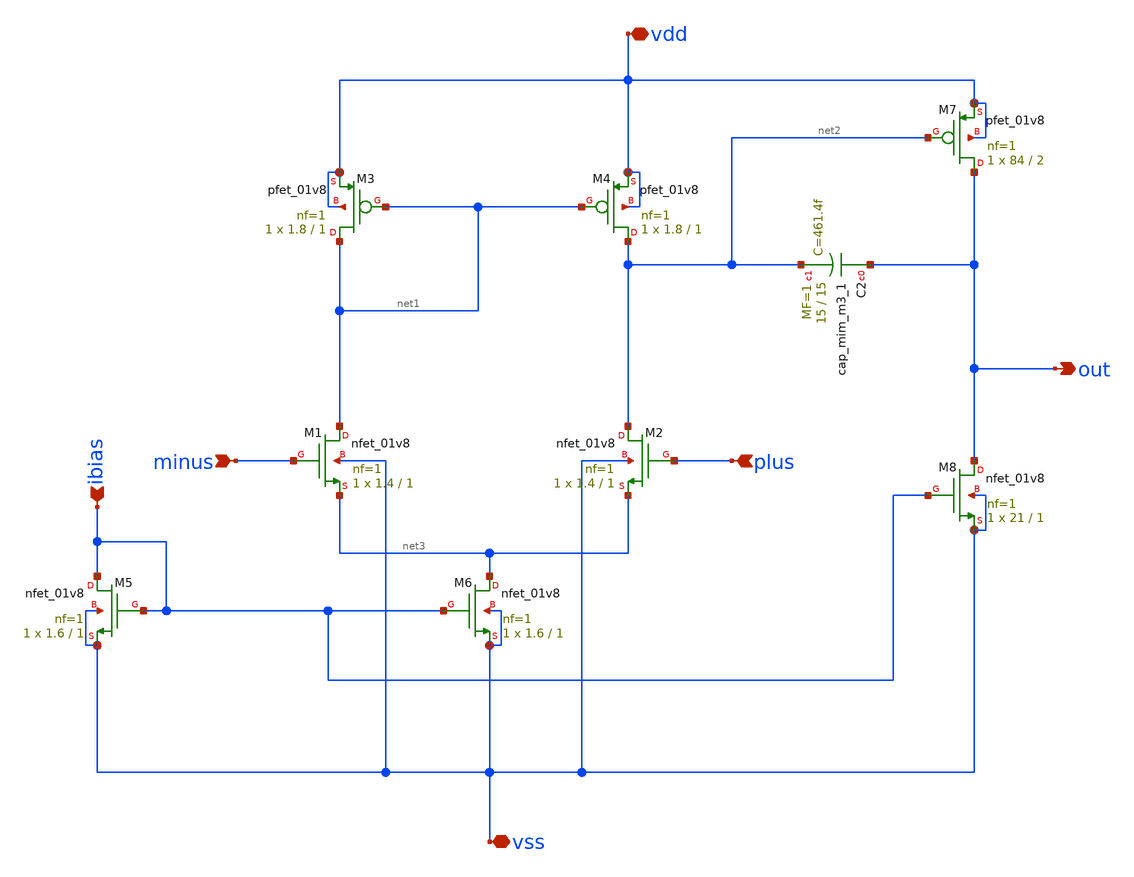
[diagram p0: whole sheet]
** sch_path: 2stageOTA.sch
**.subckt 2stageOTA minus plus ibias vdd out vss
*.ipin minus
*.ipin plus
*.ipin ibias
*.iopin vdd
*.opin out
*.iopin vss
XM1 net1 minus net3 vss sky130_fd_pr__nfet_01v8 L=1 W=1.4 nf=1 ad='int((1 + 1)/2) * 1.4 / 1 * 0.29' as='int((1 + 2)/2) * 1.4 / 1 * 0.29'
+ pd='2*int((1 + 1)/2) * (1.4 / 1 + 0.29)' ps='2*int((1 + 2)/2) * (1.4 / 1 + 0.29)' nrd='0.29 / 1.4 ' nrs='0.29 / 1.4 '
+ sa=0 sb=0 sd=0 mult=1 m=1
XM2 net2 plus net3 vss sky130_fd_pr__nfet_01v8 L=1 W=1.4 nf=1 ad='int((1 + 1)/2) * 1.4 / 1 * 0.29' as='int((1 + 2)/2) * 1.4 / 1 * 0.29'
+ pd='2*int((1 + 1)/2) * (1.4 / 1 + 0.29)' ps='2*int((1 + 2)/2) * (1.4 / 1 + 0.29)' nrd='0.29 / 1.4 ' nrs='0.29 / 1.4 '
+ sa=0 sb=0 sd=0 mult=1 m=1
XM3 net1 net1 vdd vdd sky130_fd_pr__pfet_01v8 L=1 W=1.8 nf=1 ad='int((1 + 1)/2) * 1.8 / 1 * 0.29' as='int((1 + 2)/2) * 1.8 / 1 * 0.29'
+ pd='2*int((1 + 1)/2) * (1.8 / 1 + 0.29)' ps='2*int((1 + 2)/2) * (1.8 / 1 + 0.29)' nrd='0.29 / 1.8 ' nrs='0.29 / 1.8 '
+ sa=0 sb=0 sd=0 mult=1 m=1
XM4 net2 net1 vdd vdd sky130_fd_pr__pfet_01v8 L=1 W=1.8 nf=1 ad='int((1 + 1)/2) * 1.8 / 1 * 0.29' as='int((1 + 2)/2) * 1.8 / 1 * 0.29'
+ pd='2*int((1 + 1)/2) * (1.8 / 1 + 0.29)' ps='2*int((1 + 2)/2) * (1.8 / 1 + 0.29)' nrd='0.29 / 1.8 ' nrs='0.29 / 1.8 '
+ sa=0 sb=0 sd=0 mult=1 m=1
XM5 ibias ibias vss vss sky130_fd_pr__nfet_01v8 L=1 W=1.6 nf=1 ad='int((1 + 1)/2) * 1.6 / 1 * 0.29' as='int((1 + 2)/2) * 1.6 / 1 * 0.29'
+ pd='2*int((1 + 1)/2) * (1.6 / 1 + 0.29)' ps='2*int((1 + 2)/2) * (1.6 / 1 + 0.29)' nrd='0.29 / 1.6 ' nrs='0.29 / 1.6 '
+ sa=0 sb=0 sd=0 mult=1 m=1
XM6 net3 ibias vss vss sky130_fd_pr__nfet_01v8 L=1 W=1.6 nf=1 ad='int((1 + 1)/2) * 1.6 / 1 * 0.29' as='int((1 + 2)/2) * 1.6 / 1 * 0.29'
+ pd='2*int((1 + 1)/2) * (1.6 / 1 + 0.29)' ps='2*int((1 + 2)/2) * (1.6 / 1 + 0.29)' nrd='0.29 / 1.6 ' nrs='0.29 / 1.6 '
+ sa=0 sb=0 sd=0 mult=1 m=1
XM7 out net2 vdd vdd sky130_fd_pr__pfet_01v8 L=2 W=84 nf=1 ad='int((1 + 1)/2) * 84 / 1 * 0.29' as='int((1 + 2)/2) * 84 / 1 * 0.29'
+ pd='2*int((1 + 1)/2) * (84 / 1 + 0.29)' ps='2*int((1 + 2)/2) * (84 / 1 + 0.29)' nrd='0.29 / 84 ' nrs='0.29 / 84 '
+ sa=0 sb=0 sd=0 mult=1 m=1
XM8 out ibias vss vss sky130_fd_pr__nfet_01v8 L=1 W=21 nf=1 ad='int((1 + 1)/2) * 21 / 1 * 0.29' as='int((1 + 2)/2) * 21 / 1 * 0.29'
+ pd='2*int((1 + 1)/2) * (21 / 1 + 0.29)' ps='2*int((1 + 2)/2) * (21 / 1 + 0.29)' nrd='0.29 / 21 ' nrs='0.29 / 21 '
+ sa=0 sb=0 sd=0 mult=1 m=1
XC2 out net2 sky130_fd_pr__cap_mim_m3_1 W=15 L=15 MF=1 m=1
**.ends
.end
